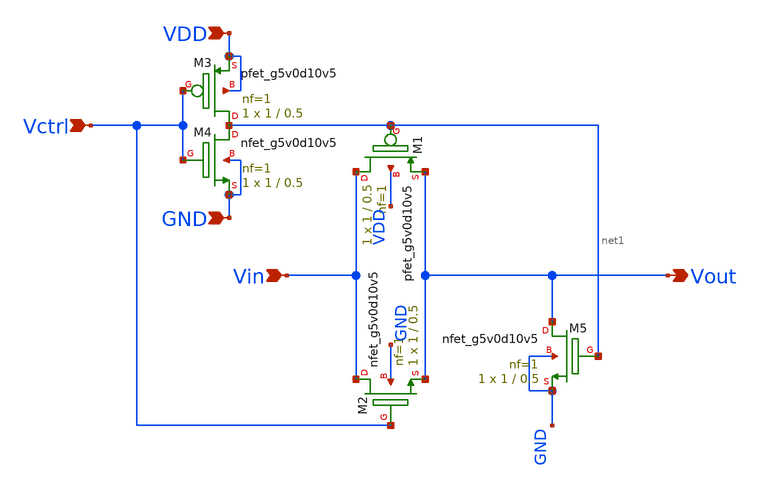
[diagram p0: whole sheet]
** sch_path: SKY130/SAR-ADC/SAR-ADC_5.0V/SW_CDAC_W1.sch
**.subckt SW_CDAC_W1 Vctrl Vin Vout VDD GND
*.ipin Vctrl
*.ipin Vin
*.opin Vout
*.ipin VDD
*.ipin GND
XM1 Vin net1 Vout VDD sky130_fd_pr__pfet_g5v0d10v5 L=0.5 W=1 nf=1 ad='int((1 + 1)/2) * 1 / 1 * 0.29'
+ as='int((1 + 2)/2) * 1 / 1 * 0.29' pd='2*int((1 + 1)/2) * (1 / 1 + 0.29)' ps='2*int((1 + 2)/2) * (1 / 1 + 0.29)'
+ nrd='0.29 / 1 ' nrs='0.29 / 1 ' sa=0 sb=0 sd=0 mult=1 m=1
XM2 Vin Vctrl Vout GND sky130_fd_pr__nfet_g5v0d10v5 L=0.5 W=1 nf=1 ad='int((1 + 1)/2) * 1 / 1 * 0.29'
+ as='int((1 + 2)/2) * 1 / 1 * 0.29' pd='2*int((1 + 1)/2) * (1 / 1 + 0.29)' ps='2*int((1 + 2)/2) * (1 / 1 + 0.29)'
+ nrd='0.29 / 1 ' nrs='0.29 / 1 ' sa=0 sb=0 sd=0 mult=1 m=1
XM3 net1 Vctrl VDD VDD sky130_fd_pr__pfet_g5v0d10v5 L=0.5 W=1 nf=1 ad='int((1 + 1)/2) * 1 / 1 * 0.29'
+ as='int((1 + 2)/2) * 1 / 1 * 0.29' pd='2*int((1 + 1)/2) * (1 / 1 + 0.29)' ps='2*int((1 + 2)/2) * (1 / 1 + 0.29)'
+ nrd='0.29 / 1 ' nrs='0.29 / 1 ' sa=0 sb=0 sd=0 mult=1 m=1
XM4 net1 Vctrl GND GND sky130_fd_pr__nfet_g5v0d10v5 L=0.5 W=1 nf=1 ad='int((1 + 1)/2) * 1 / 1 * 0.29'
+ as='int((1 + 2)/2) * 1 / 1 * 0.29' pd='2*int((1 + 1)/2) * (1 / 1 + 0.29)' ps='2*int((1 + 2)/2) * (1 / 1 + 0.29)'
+ nrd='0.29 / 1 ' nrs='0.29 / 1 ' sa=0 sb=0 sd=0 mult=1 m=1
XM5 Vout net1 GND GND sky130_fd_pr__nfet_g5v0d10v5 L=0.5 W=1 nf=1 ad='int((1 + 1)/2) * 1 / 1 * 0.29'
+ as='int((1 + 2)/2) * 1 / 1 * 0.29' pd='2*int((1 + 1)/2) * (1 / 1 + 0.29)' ps='2*int((1 + 2)/2) * (1 / 1 + 0.29)'
+ nrd='0.29 / 1 ' nrs='0.29 / 1 ' sa=0 sb=0 sd=0 mult=1 m=1
**.ends
.end
